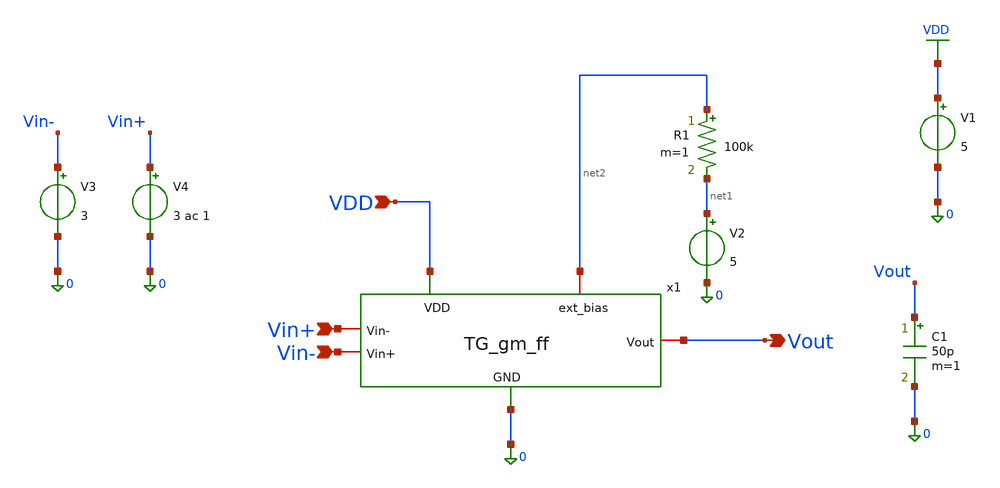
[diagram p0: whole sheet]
** sch_path: TG_gm_ff/TG_gm_ff_testing.sch
**.subckt TG_gm_ff_testing VDD Vin- Vin+ Vout
*.ipin VDD
*.ipin Vin-
*.ipin Vin+
*.opin Vout
V1 VDD 0 5
V3 Vin- 0 3
V4 Vin+ 0 3 ac 1
R1 net2 net1 100k m=1
V2 net1 0 5
C1 Vout 0 50p m=1
x1 VDD Vout Vin+ Vin- net2 0 TG_gm_ff
**** begin user architecture code



*==============================================================================
* TG_gm_ff  -  5T OTA transconductance / gain characterisation
*
* Sweeps the external bias network R1 (10 ohm .. 100 Meg, 1-2-4-8 per decade)
* against V2 (0.5 .. 5 V) and extracts, at every point:
*
*     Gm(f)   = Iout,short / Vid      <- the transconductance on its own
*     Zout(f) = output impedance incl. CL
*     Av(f)   = Gm * Zout             <- the loaded voltage gain
*
* Method: TWO ac analyses per bias point, sharing one operating point.
*   run A - differential drive on the inputs, Itest off        -> Av(f)
*   run B - inputs ac-grounded, 1 A ac injected at Vout        -> Zout(f)
*   then  Gm(f) = Av(f) / Zout(f), exact at every frequency.
*
* A single ac run (as in the original deck) can only ever give you the product
* Gm*Zout, never the two factors separately.
*
* Run with:   ngspice -i tg_gm_ff_sweep.spice
*   (use -i, not -b, so the plot windows appear)
*==============================================================================

.include /foss/pdks/gf180mcuD/libs.tech/ngspice/design.ngspice
.lib /foss/pdks/gf180mcuD/libs.tech/ngspice/sm141064.ngspice typical
.lib /foss/pdks/gf180mcuD/libs.tech/ngspice/sm141064.ngspice res_typical
.lib /foss/pdks/gf180mcuD/libs.tech/ngspice/sm141064.ngspice moscap_typical
.lib /foss/pdks/gf180mcuD/libs.tech/ngspice/sm141064.ngspice mimcap_typical

* nominal device behaviour - no statistical spread on the sweep
.param sw_stat_global=0
.param sw_stat_mismatch=0

*==============================================================================
* Test sources
*==============================================================================
V1 VDD 0 5

* Differential AC drive: vid = v(Vin+) - v(Vin-) = 1 V, common mode = 3 V.
* Your original deck drove Vin+ with ac 1 single-ended; that mixes in a common
* mode of 0.5 V. Differential drive gives Gm and Av directly, no CM error.
V3 Vin- 0 3 ac 0.5 180
V4 Vin+ 0 3 ac 0.5 0

* External bias network (swept)
R1 net2 net1 100k
V2 net1 0 5

C1 Vout 0 50p

* AC-only probe current for the Zout measurement. dc 0 -> operating point
* is identical in both AC runs.
Itest 0 Vout dc 0 ac 0

x1 VDD Vout Vin+ Vin- net2 0 TG_gm_ff

*==============================================================================
* DUT
*
* NOTE ON PIN ORDER: the subckt header below is  VDD Vout Vin- Vin+ ext_bias GND
* but the instance above is  VDD Vout Vin+ Vin- net2 0.  Position 3 carries the
* top-level net Vin+ into the port named Vin- (the gate of XM8, the
* output-side device).  As netlisted, the source labelled Vin+ drives the
* INVERTING input, so Av is negative.  That is why the Gm expression below
* carries a minus sign.  If you fix the pin order, drop the minus sign.
*==============================================================================
.subckt TG_gm_ff VDD Vout Vin- Vin+ ext_bias GND
XC3 ext_bias GND cap_nmos_06v0 c_width=60e-6 c_length=10e-6 m=6
XC1 VDD GND cap_nmos_06v0 c_width=60e-6 c_length=10e-6 m=6
XM7 net2 ext_bias GND GND nfet_05v0 L=1.2u W=16u nf=8 ad='int((nf+1)/2) * W/nf * 0.18u' as='int((nf+2)/2) * W/nf * 0.18u'
+ pd='2*int((nf+1)/2) * (W/nf + 0.18u)'  ps='2*int((nf+2)/2) * (W/nf + 0.18u)' nrd='0.18u / W' nrs='0.18u / W'
+ sa=0 sb=0 sd=0 m=2
XM8 Vout Vin- net2 GND nfet_05v0 L=1u W=7.5u nf=4 ad='int((nf+1)/2) * W/nf * 0.18u' as='int((nf+2)/2) * W/nf * 0.18u'
+ pd='2*int((nf+1)/2) * (W/nf + 0.18u)'  ps='2*int((nf+2)/2) * (W/nf + 0.18u)' nrd='0.18u / W' nrs='0.18u / W'
+ sa=0 sb=0 sd=0 m=4
XM9 net1 net1 VDD VDD pfet_05v0 L=2u W=17u nf=10 ad='int((nf+1)/2) * W/nf * 0.18u' as='int((nf+2)/2) * W/nf * 0.18u'
+ pd='2*int((nf+1)/2) * (W/nf + 0.18u)'  ps='2*int((nf+2)/2) * (W/nf + 0.18u)' nrd='0.18u / W' nrs='0.18u / W'
+ sa=0 sb=0 sd=0 m=2
XM5 ext_bias ext_bias GND GND nfet_05v0 L=1.2u W=16u nf=8 ad='int((nf+1)/2) * W/nf * 0.18u' as='int((nf+2)/2) * W/nf * 0.18u'
+ pd='2*int((nf+1)/2) * (W/nf + 0.18u)'  ps='2*int((nf+2)/2) * (W/nf + 0.18u)' nrd='0.18u / W' nrs='0.18u / W'
+ sa=0 sb=0 sd=0 m=2
XM1 net1 Vin+ net2 GND nfet_05v0 L=1u W=7.5u nf=4 ad='int((nf+1)/2) * W/nf * 0.18u' as='int((nf+2)/2) * W/nf * 0.18u'
+ pd='2*int((nf+1)/2) * (W/nf + 0.18u)'  ps='2*int((nf+2)/2) * (W/nf + 0.18u)' nrd='0.18u / W' nrs='0.18u / W'
+ sa=0 sb=0 sd=0 m=4
XM2 Vout net1 VDD VDD pfet_05v0 L=2u W=17u nf=10 ad='int((nf+1)/2) * W/nf * 0.18u' as='int((nf+2)/2) * W/nf * 0.18u'
+ pd='2*int((nf+1)/2) * (W/nf + 0.18u)'  ps='2*int((nf+2)/2) * (W/nf + 0.18u)' nrd='0.18u / W' nrs='0.18u / W'
+ sa=0 sb=0 sd=0 m=2
.ends

*==============================================================================
.control

*------------------------------------------------------------------ user knobs
set rsweep = ( 10 20 40 80 100 200 400 800 1000 2000 4000 8000 10000 20000 40000 80000 100000 200000
+ 400000 800000 1000000 2000000 4000000 8000000 10000000 20000000 40000000 80000000 100000000 )
set vsweep = ( 0.5 1 1.5 2 3 4 5 )
set fstart = 0.1
set fstop  = 1G
set fppd   = 20                       $ ac points per decade

set plot_gm_mag                       $ unset any of these to skip that plot
set plot_gm_ph
set plot_av_mag
set plot_av_ph

set csvfile = ./tg_gm_ff_sweep_summary.csv
*-----------------------------------------------------------------------------

set noaskquit

echo
echo
+ V2,R1,Ibias,Itail,Vout,Vnet1,Gm_S,Gm_dBS,Gain_dB,Zout_ohm,f3dB_Hz,UGBW_Hz,fGm_5deg_Hz,GmHF_ratio > $csvfile

foreach vb $vsweep
  alter @v2[dc] = $vb

  * one storage plot per V2 so the vector names can be reused
  setplot new
  set store = $curplot

  echo
  echo
+ |==================================================================================================
  echo |


**** end user architecture code
**.ends
.GLOBAL VDD
.end
